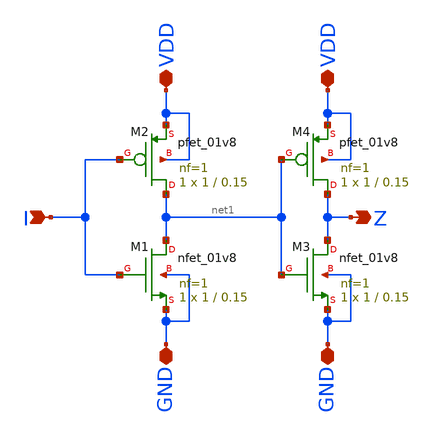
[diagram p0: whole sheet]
** sch_path: sky130_cells/Practice/Example_Inverter/Buffer.sch
**.subckt Buffer I VDD GND VDD GND Z
*.ipin I
*.iopin VDD
*.iopin GND
*.iopin VDD
*.iopin GND
*.opin Z
XM1 net1 I GND GND sky130_fd_pr__nfet_01v8 L=0.15 W=1 nf=1 ad='int((nf+1)/2) * W/nf * 0.29' as='int((nf+2)/2) * W/nf * 0.29'
+ pd='2*int((nf+1)/2) * (W/nf + 0.29)' ps='2*int((nf+2)/2) * (W/nf + 0.29)' nrd='0.29 / W' nrs='0.29 / W'
+ sa=0 sb=0 sd=0 mult=1 m=1
XM2 net1 I VDD VDD sky130_fd_pr__pfet_01v8 L=0.15 W=1 nf=1 ad='int((nf+1)/2) * W/nf * 0.29' as='int((nf+2)/2) * W/nf * 0.29'
+ pd='2*int((nf+1)/2) * (W/nf + 0.29)' ps='2*int((nf+2)/2) * (W/nf + 0.29)' nrd='0.29 / W' nrs='0.29 / W'
+ sa=0 sb=0 sd=0 mult=1 m=1
XM3 Z net1 GND GND sky130_fd_pr__nfet_01v8 L=0.15 W=1 nf=1 ad='int((nf+1)/2) * W/nf * 0.29' as='int((nf+2)/2) * W/nf * 0.29'
+ pd='2*int((nf+1)/2) * (W/nf + 0.29)' ps='2*int((nf+2)/2) * (W/nf + 0.29)' nrd='0.29 / W' nrs='0.29 / W'
+ sa=0 sb=0 sd=0 mult=1 m=1
XM4 Z net1 VDD VDD sky130_fd_pr__pfet_01v8 L=0.15 W=1 nf=1 ad='int((nf+1)/2) * W/nf * 0.29' as='int((nf+2)/2) * W/nf * 0.29'
+ pd='2*int((nf+1)/2) * (W/nf + 0.29)' ps='2*int((nf+2)/2) * (W/nf + 0.29)' nrd='0.29 / W' nrs='0.29 / W'
+ sa=0 sb=0 sd=0 mult=1 m=1
**.ends
.end
